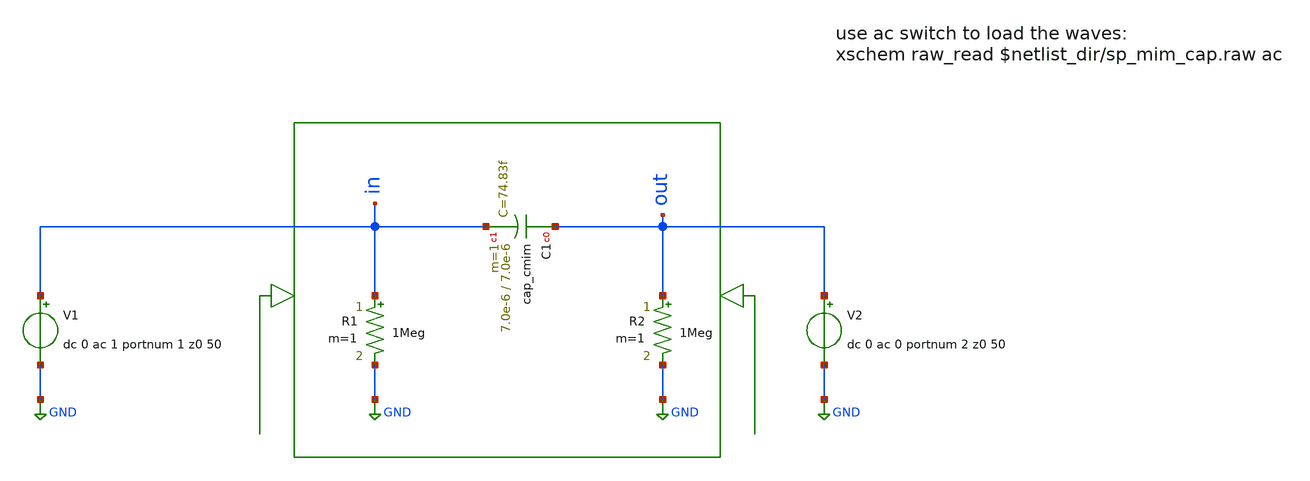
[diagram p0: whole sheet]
** sch_path: ihp-sg13g2/xschem_libs/sg13g2_tests_ase/sp_mim_cap/schematic/sp_mim_cap.sch
* Copyright 2021 Stefan Frederik Schippers
* Licensed under the Apache License, Version 2.0 (the "License");
* you may not use this file except in compliance with the License.
* You may obtain a copy of the License at
* https://www.apache.org/licenses/LICENSE-2.0
* Unless required by applicable law or agreed to in writing, software
* distributed under the License is distributed on an "AS IS" BASIS,
* WITHOUT WARRANTIES OR CONDITIONS OF ANY KIND, either express or implied.
* See the License for the specific language governing permissions and
* limitations under the License.
* Copyright 2023 IHP PDK Authors
**.subckt sp_mim_cap
R1 in GND 1Meg m=1
V1 in GND dc 0 ac 1 portnum 1 z0 50
R2 out GND 1Meg m=1
V2 out GND dc 0 ac 0 portnum 2 z0 50
XC1 out in cap_cmim w=7.0e-6 l=7.0e-6 m=1 mm_ok=1
**.ends
.GLOBAL GND
.end
